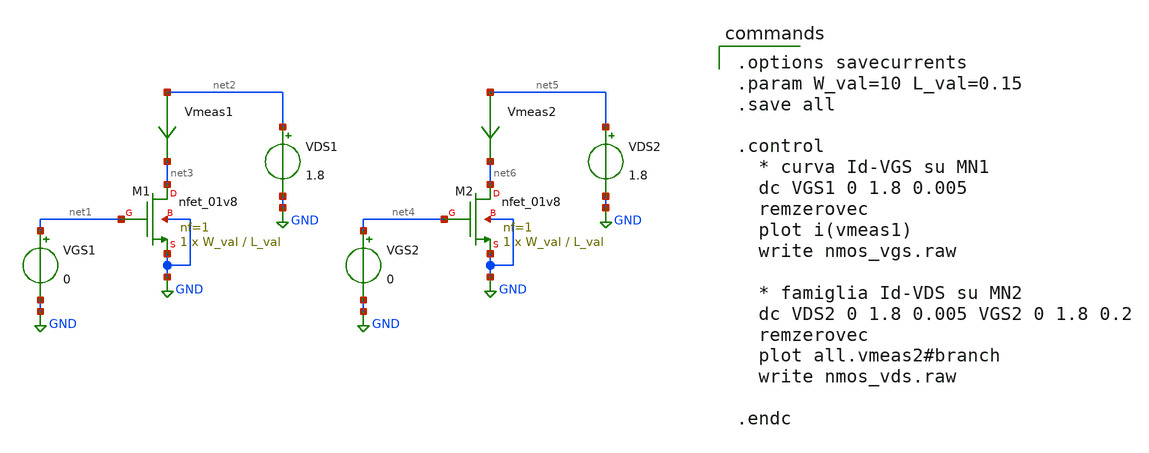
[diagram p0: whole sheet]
** sch_path: 01_xschem_ngspice/soluzioni/lab02/xschem/nmos_char.sch
**.subckt nmos_char
XM1 net3 net1 GND GND sky130_fd_pr__nfet_01v8 L=L_val W=W_val nf=1 ad='int((1 + 1)/2) * W_val / 1 * 0.29'
+ as='int((1 + 2)/2) * W_val / 1 * 0.29' pd='2*int((1 + 1)/2) * (W_val / 1 + 0.29)' ps='2*int((1 + 2)/2) * (W_val / 1 + 0.29)'
+ nrd='0.29 / W_val ' nrs='0.29 / W_val ' sa=0 sb=0 sd=0 mult=1 m=1
VGS1 net1 GND 0
VDS1 net2 GND 1.8
XM2 net6 net4 GND GND sky130_fd_pr__nfet_01v8 L=L_val W=W_val nf=1 ad='int((1 + 1)/2) * W_val / 1 * 0.29'
+ as='int((1 + 2)/2) * W_val / 1 * 0.29' pd='2*int((1 + 1)/2) * (W_val / 1 + 0.29)' ps='2*int((1 + 2)/2) * (W_val / 1 + 0.29)'
+ nrd='0.29 / W_val ' nrs='0.29 / W_val ' sa=0 sb=0 sd=0 mult=1 m=1
VGS2 net4 GND 0
VDS2 net5 GND 1.8
Vmeas2 net5 net6 0
.save i(vmeas2)
Vmeas1 net2 net3 0
.save i(vmeas1)
**** begin user architecture code

** opencircuitdesign pdks install
.lib $::SKYWATER_MODELS/sky130.lib.spice tt


.options savecurrents
.param W_val=10 L_val=0.15
.save all

.control
  * curva Id-VGS su MN1
  dc VGS1 0 1.8 0.005
  remzerovec
  plot i(vmeas1)
  write nmos_vgs.raw

  * famiglia Id-VDS su MN2
  dc VDS2 0 1.8 0.005 VGS2 0 1.8 0.2
  remzerovec
  plot all.vmeas2#branch
  write nmos_vds.raw

.endc

**** end user architecture code
**.ends
.GLOBAL GND
.end
